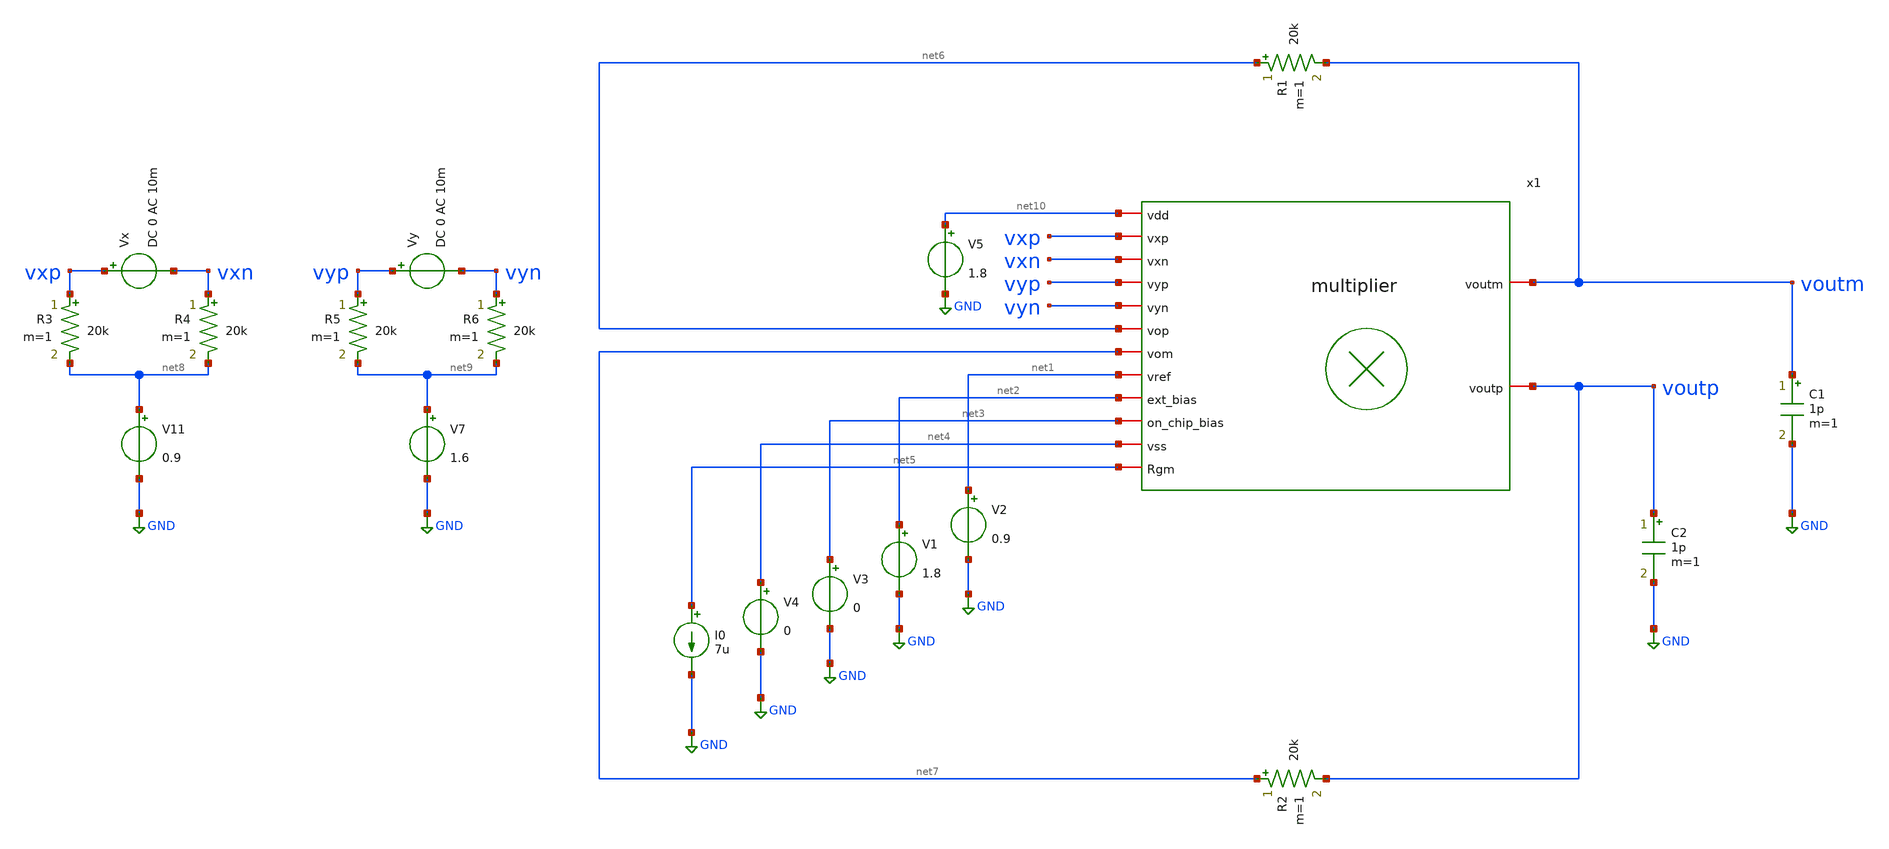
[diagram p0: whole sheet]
** sch_path: LVS/Unic_cass_final_design_lvs/Simulations/Multiplier/Testbenches/multiplier_tb.sch
**.subckt multiplier_tb
x1 net10 vxp vxn net4 net3 vyp net2 vyn net6 voutm net7 voutp net1 net5 multiplier
V5 net10 GND 1.8
V2 net1 GND 0.9
V1 net2 GND 1.8
V3 net3 GND 0
V4 net4 GND 0
R1 net6 voutm 20k m=1
R2 net7 voutp 20k m=1
C1 voutm GND 1p m=1
C2 voutp GND 1p m=1
V11 net8 GND 0.9
R3 vxp net8 20k m=1
R4 vxn net8 20k m=1
Vx vxp vxn DC 0 AC 10m
V7 net9 GND 1.6
R5 vyp net9 20k m=1
R6 vyn net9 20k m=1
Vy vyp vyn DC 0 AC 10m
I0 net5 GND 7u
**** begin user architecture code



.lib cornerMOSlv.lib mos_tt
.lib cornerMOShv.lib mos_tt
.lib cornerHBT.lib hbt_typ
.lib cornerRES.lib res_typ
.lib cornerCAP.lib cap_typ



**** end user architecture code
**.ends
.GLOBAL GND
**** begin user architecture code



.options savecurrents

.control
save all



op
*dc Vy -0.1 0.1 0.05 Vx -0.1 0.1 0.05
*tran 10n 10u


let vdiff = v(voutp)-v(voutm)
let vin= v(vp)-v(vm)
*plot db(vdiff/vin) (180/pi)*phase(vdiff/vin)
plot vdiff
write multiplier_tb.raw

.endc



**** end user architecture code
.end
